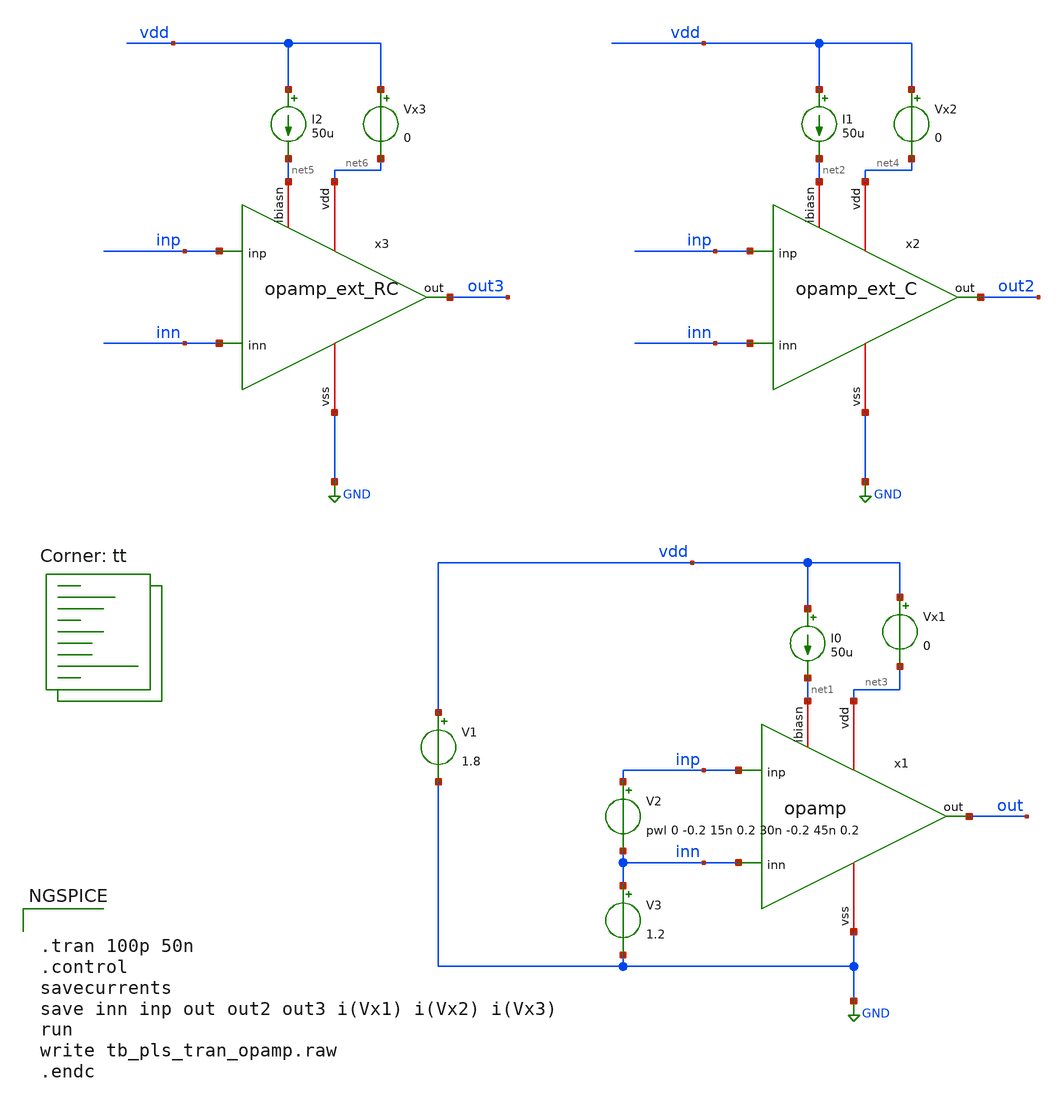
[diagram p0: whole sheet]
** sch_path: sky130A/HelloWorld/analog/schematic/tb_pls_tran_opamp.sch
**.subckt tb_pls_tran_opamp
x1 net3 out inp inn net1 GND opamp
V1 vdd GND 1.8
I0 vdd net1 50u
V2 inp inn pwl 0 -0.2 15n 0.2 30n -0.2 45n 0.2
V3 inn GND 1.2
x2 net4 out2 inp inn net2 GND opamp_ext_C
I1 vdd net2 50u
Vx1 vdd net3 0
.save i(vx1)
Vx2 vdd net4 0
.save i(vx2)
x3 net6 out3 inp inn net5 GND opamp_ext_RC
I2 vdd net5 50u
Vx3 vdd net6 0
.save i(vx3)
**** begin user architecture code
.lib $::SKYWATER_MODELS/sky130.lib.spice tt


.tran 100p 50n
.control
savecurrents
save inn inp out out2 out3 i(Vx1) i(Vx2) i(Vx3)
run
write tb_pls_tran_opamp.raw
.endc


**** end user architecture code
**.ends

* expanding   symbol:  opamp.sym # of pins=6
** sym_path: sky130A/HelloWorld/xschem/opamp.sym
** sch_path: sky130A/HelloWorld/xschem/opamp.sch
.subckt opamp vdd out inp inn ibiasn vss
*.ipin inn
*.ipin inp
*.iopin vdd
*.iopin vss
*.iopin ibiasn
*.opin out
XM1 pbias inn tail vss sky130_fd_pr__nfet_01v8 L=1 W=40 nf=1 ad='int((nf+1)/2) * W/nf * 0.29' as='int((nf+2)/2) * W/nf * 0.29'
+ pd='2*int((nf+1)/2) * (W/nf + 0.29)' ps='2*int((nf+2)/2) * (W/nf + 0.29)' nrd='0.29 / W' nrs='0.29 / W'
+ sa=0 sb=0 sd=0 mult=1 m=1
XM2 outz inp tail vss sky130_fd_pr__nfet_01v8 L=1 W=40 nf=1 ad='int((nf+1)/2) * W/nf * 0.29' as='int((nf+2)/2) * W/nf * 0.29'
+ pd='2*int((nf+1)/2) * (W/nf + 0.29)' ps='2*int((nf+2)/2) * (W/nf + 0.29)' nrd='0.29 / W' nrs='0.29 / W'
+ sa=0 sb=0 sd=0 mult=1 m=1
XM3 pbias pbias vdd vdd sky130_fd_pr__pfet_01v8 L=0.5 W=20 nf=1 ad='int((nf+1)/2) * W/nf * 0.29' as='int((nf+2)/2) * W/nf * 0.29'
+ pd='2*int((nf+1)/2) * (W/nf + 0.29)' ps='2*int((nf+2)/2) * (W/nf + 0.29)' nrd='0.29 / W' nrs='0.29 / W'
+ sa=0 sb=0 sd=0 mult=1 m=1
XM4 outz pbias vdd vdd sky130_fd_pr__pfet_01v8 L=0.5 W=20 nf=1 ad='int((nf+1)/2) * W/nf * 0.29' as='int((nf+2)/2) * W/nf * 0.29'
+ pd='2*int((nf+1)/2) * (W/nf + 0.29)' ps='2*int((nf+2)/2) * (W/nf + 0.29)' nrd='0.29 / W' nrs='0.29 / W'
+ sa=0 sb=0 sd=0 mult=1 m=1
XM5 out outz vdd vdd sky130_fd_pr__pfet_01v8 L=0.5 W=20 nf=1 ad='int((nf+1)/2) * W/nf * 0.29' as='int((nf+2)/2) * W/nf * 0.29'
+ pd='2*int((nf+1)/2) * (W/nf + 0.29)' ps='2*int((nf+2)/2) * (W/nf + 0.29)' nrd='0.29 / W' nrs='0.29 / W'
+ sa=0 sb=0 sd=0 mult=1 m=1
XM6[1] tail ibiasn vss vss sky130_fd_pr__nfet_01v8 L=1 W=40 nf=1 ad='int((nf+1)/2) * W/nf * 0.29' as='int((nf+2)/2) * W/nf * 0.29'
+ pd='2*int((nf+1)/2) * (W/nf + 0.29)' ps='2*int((nf+2)/2) * (W/nf + 0.29)' nrd='0.29 / W' nrs='0.29 / W'
+ sa=0 sb=0 sd=0 mult=1 m=1
XM6[0] tail ibiasn vss vss sky130_fd_pr__nfet_01v8 L=1 W=40 nf=1 ad='int((nf+1)/2) * W/nf * 0.29' as='int((nf+2)/2) * W/nf * 0.29'
+ pd='2*int((nf+1)/2) * (W/nf + 0.29)' ps='2*int((nf+2)/2) * (W/nf + 0.29)' nrd='0.29 / W' nrs='0.29 / W'
+ sa=0 sb=0 sd=0 mult=1 m=1
XM7 out ibiasn vss vss sky130_fd_pr__nfet_01v8 L=1 W=40 nf=1 ad='int((nf+1)/2) * W/nf * 0.29' as='int((nf+2)/2) * W/nf * 0.29'
+ pd='2*int((nf+1)/2) * (W/nf + 0.29)' ps='2*int((nf+2)/2) * (W/nf + 0.29)' nrd='0.29 / W' nrs='0.29 / W'
+ sa=0 sb=0 sd=0 mult=1 m=1
XM8 ibiasn ibiasn vss vss sky130_fd_pr__nfet_01v8 L=1 W=40 nf=1 ad='int((nf+1)/2) * W/nf * 0.29' as='int((nf+2)/2) * W/nf * 0.29'
+ pd='2*int((nf+1)/2) * (W/nf + 0.29)' ps='2*int((nf+2)/2) * (W/nf + 0.29)' nrd='0.29 / W' nrs='0.29 / W'
+ sa=0 sb=0 sd=0 mult=1 m=1
.ends


* expanding   symbol:  opamp_ext_C.sym # of pins=6
** sym_path: sky130A/HelloWorld/xschem/opamp.sym
.include $env(HOME)/design_workspace/sky130A/HelloWorld/analog/layout/opamp_ext_C.spice

* expanding   symbol:  opamp_ext_RC.sym # of pins=6
** sym_path: sky130A/HelloWorld/xschem/opamp.sym
.include $env(HOME)/design_workspace/sky130A/HelloWorld/analog/layout/opamp_ext_RC.spice
.GLOBAL GND
.end
